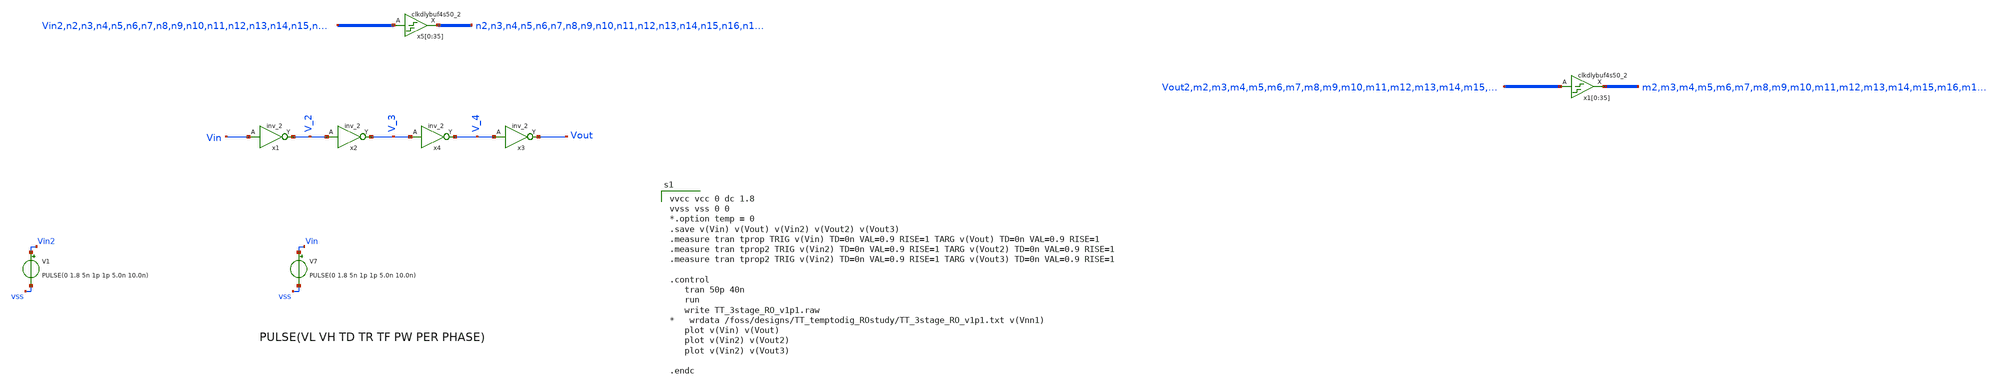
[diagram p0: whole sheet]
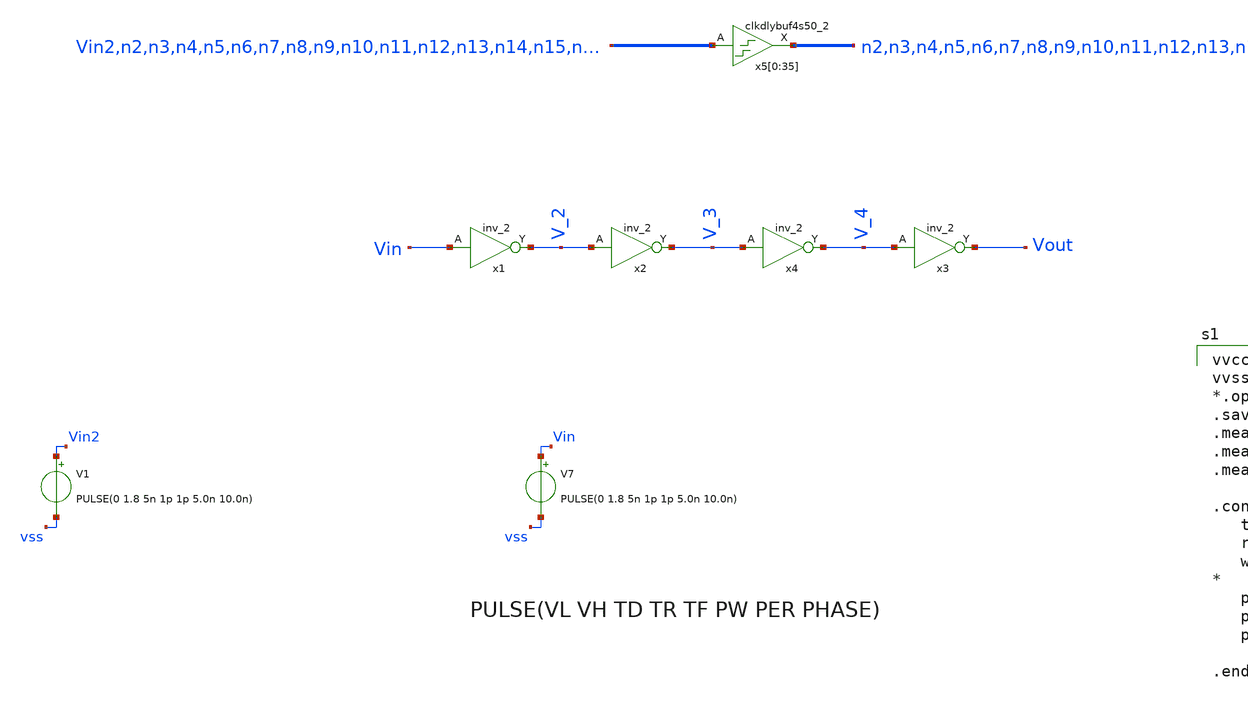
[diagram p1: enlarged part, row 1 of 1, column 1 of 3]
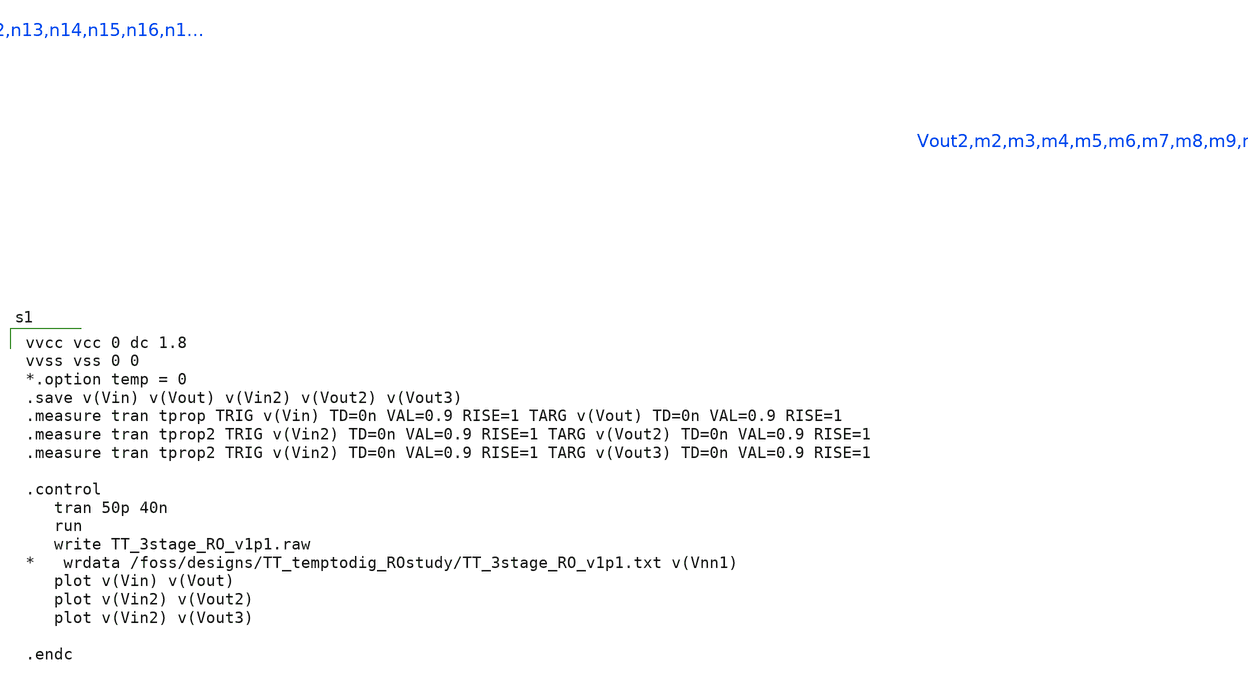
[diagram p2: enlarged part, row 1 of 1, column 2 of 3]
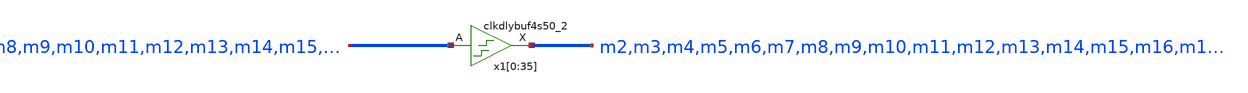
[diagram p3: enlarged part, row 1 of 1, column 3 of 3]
** sch_path: LS_boot_20230921/sch/TDC_test_buf.sch
.lib $::SKYWATER_MODELS/sky130.lib.spice tt
.include $::SKYWATER_STDCELLS/sky130_fd_sc_hd.spice

**.subckt TDC_test_buf
x1 Vin VSS VSS VCC VCC V_2 sky130_fd_sc_hd__inv_2
x2 V_2 VSS VSS VCC VCC V_3 sky130_fd_sc_hd__inv_2
x3 V_4 VSS VSS VCC VCC Vout sky130_fd_sc_hd__inv_2
V7 Vin vss PULSE(0 1.8 5n 1p 1p 5.0n 10.0n)
x4 V_3 VSS VSS VCC VCC V_4 sky130_fd_sc_hd__inv_2
V1 Vin2 vss PULSE(0 1.8 5n 1p 1p 5.0n 10.0n)
x5[0] Vin2 VSS VSS VCC VCC n2 sky130_fd_sc_hd__clkdlybuf4s50_2
x5[1] n2 VSS VSS VCC VCC n3 sky130_fd_sc_hd__clkdlybuf4s50_2
x5[2] n3 VSS VSS VCC VCC n4 sky130_fd_sc_hd__clkdlybuf4s50_2
x5[3] n4 VSS VSS VCC VCC n5 sky130_fd_sc_hd__clkdlybuf4s50_2
x5[4] n5 VSS VSS VCC VCC n6 sky130_fd_sc_hd__clkdlybuf4s50_2
x5[5] n6 VSS VSS VCC VCC n7 sky130_fd_sc_hd__clkdlybuf4s50_2
x5[6] n7 VSS VSS VCC VCC n8 sky130_fd_sc_hd__clkdlybuf4s50_2
x5[7] n8 VSS VSS VCC VCC n9 sky130_fd_sc_hd__clkdlybuf4s50_2
x5[8] n9 VSS VSS VCC VCC n10 sky130_fd_sc_hd__clkdlybuf4s50_2
x5[9] n10 VSS VSS VCC VCC n11 sky130_fd_sc_hd__clkdlybuf4s50_2
x5[10] n11 VSS VSS VCC VCC n12 sky130_fd_sc_hd__clkdlybuf4s50_2
x5[11] n12 VSS VSS VCC VCC n13 sky130_fd_sc_hd__clkdlybuf4s50_2
x5[12] n13 VSS VSS VCC VCC n14 sky130_fd_sc_hd__clkdlybuf4s50_2
x5[13] n14 VSS VSS VCC VCC n15 sky130_fd_sc_hd__clkdlybuf4s50_2
x5[14] n15 VSS VSS VCC VCC n16 sky130_fd_sc_hd__clkdlybuf4s50_2
x5[15] n16 VSS VSS VCC VCC n17 sky130_fd_sc_hd__clkdlybuf4s50_2
x5[16] n17 VSS VSS VCC VCC n18 sky130_fd_sc_hd__clkdlybuf4s50_2
x5[17] n18 VSS VSS VCC VCC n19 sky130_fd_sc_hd__clkdlybuf4s50_2
x5[18] n19 VSS VSS VCC VCC n20 sky130_fd_sc_hd__clkdlybuf4s50_2
x5[19] n20 VSS VSS VCC VCC n21 sky130_fd_sc_hd__clkdlybuf4s50_2
x5[20] n21 VSS VSS VCC VCC n22 sky130_fd_sc_hd__clkdlybuf4s50_2
x5[21] n22 VSS VSS VCC VCC n23 sky130_fd_sc_hd__clkdlybuf4s50_2
x5[22] n23 VSS VSS VCC VCC n24 sky130_fd_sc_hd__clkdlybuf4s50_2
x5[23] n24 VSS VSS VCC VCC n25 sky130_fd_sc_hd__clkdlybuf4s50_2
x5[24] n25 VSS VSS VCC VCC n26 sky130_fd_sc_hd__clkdlybuf4s50_2
x5[25] n26 VSS VSS VCC VCC n27 sky130_fd_sc_hd__clkdlybuf4s50_2
x5[26] n27 VSS VSS VCC VCC n28 sky130_fd_sc_hd__clkdlybuf4s50_2
x5[27] n28 VSS VSS VCC VCC n29 sky130_fd_sc_hd__clkdlybuf4s50_2
x5[28] n29 VSS VSS VCC VCC n30 sky130_fd_sc_hd__clkdlybuf4s50_2
x5[29] n30 VSS VSS VCC VCC n31 sky130_fd_sc_hd__clkdlybuf4s50_2
x5[30] n31 VSS VSS VCC VCC n32 sky130_fd_sc_hd__clkdlybuf4s50_2
x5[31] n32 VSS VSS VCC VCC n33 sky130_fd_sc_hd__clkdlybuf4s50_2
x5[32] n33 VSS VSS VCC VCC n34 sky130_fd_sc_hd__clkdlybuf4s50_2
x5[33] n34 VSS VSS VCC VCC n35 sky130_fd_sc_hd__clkdlybuf4s50_2
x5[34] n35 VSS VSS VCC VCC n36 sky130_fd_sc_hd__clkdlybuf4s50_2
x5[35] n36 VSS VSS VCC VCC Vout2 sky130_fd_sc_hd__clkdlybuf4s50_2
x1[0] Vout2 VSS VSS VCC VCC m2 sky130_fd_sc_hd__clkdlybuf4s50_2
x1[1] m2 VSS VSS VCC VCC m3 sky130_fd_sc_hd__clkdlybuf4s50_2
x1[2] m3 VSS VSS VCC VCC m4 sky130_fd_sc_hd__clkdlybuf4s50_2
x1[3] m4 VSS VSS VCC VCC m5 sky130_fd_sc_hd__clkdlybuf4s50_2
x1[4] m5 VSS VSS VCC VCC m6 sky130_fd_sc_hd__clkdlybuf4s50_2
x1[5] m6 VSS VSS VCC VCC m7 sky130_fd_sc_hd__clkdlybuf4s50_2
x1[6] m7 VSS VSS VCC VCC m8 sky130_fd_sc_hd__clkdlybuf4s50_2
x1[7] m8 VSS VSS VCC VCC m9 sky130_fd_sc_hd__clkdlybuf4s50_2
x1[8] m9 VSS VSS VCC VCC m10 sky130_fd_sc_hd__clkdlybuf4s50_2
x1[9] m10 VSS VSS VCC VCC m11 sky130_fd_sc_hd__clkdlybuf4s50_2
x1[10] m11 VSS VSS VCC VCC m12 sky130_fd_sc_hd__clkdlybuf4s50_2
x1[11] m12 VSS VSS VCC VCC m13 sky130_fd_sc_hd__clkdlybuf4s50_2
x1[12] m13 VSS VSS VCC VCC m14 sky130_fd_sc_hd__clkdlybuf4s50_2
x1[13] m14 VSS VSS VCC VCC m15 sky130_fd_sc_hd__clkdlybuf4s50_2
x1[14] m15 VSS VSS VCC VCC m16 sky130_fd_sc_hd__clkdlybuf4s50_2
x1[15] m16 VSS VSS VCC VCC m17 sky130_fd_sc_hd__clkdlybuf4s50_2
x1[16] m17 VSS VSS VCC VCC m18 sky130_fd_sc_hd__clkdlybuf4s50_2
x1[17] m18 VSS VSS VCC VCC m19 sky130_fd_sc_hd__clkdlybuf4s50_2
x1[18] m19 VSS VSS VCC VCC m20 sky130_fd_sc_hd__clkdlybuf4s50_2
x1[19] m20 VSS VSS VCC VCC m21 sky130_fd_sc_hd__clkdlybuf4s50_2
x1[20] m21 VSS VSS VCC VCC m22 sky130_fd_sc_hd__clkdlybuf4s50_2
x1[21] m22 VSS VSS VCC VCC m23 sky130_fd_sc_hd__clkdlybuf4s50_2
x1[22] m23 VSS VSS VCC VCC m24 sky130_fd_sc_hd__clkdlybuf4s50_2
x1[23] m24 VSS VSS VCC VCC m25 sky130_fd_sc_hd__clkdlybuf4s50_2
x1[24] m25 VSS VSS VCC VCC m26 sky130_fd_sc_hd__clkdlybuf4s50_2
x1[25] m26 VSS VSS VCC VCC m27 sky130_fd_sc_hd__clkdlybuf4s50_2
x1[26] m27 VSS VSS VCC VCC m28 sky130_fd_sc_hd__clkdlybuf4s50_2
x1[27] m28 VSS VSS VCC VCC m29 sky130_fd_sc_hd__clkdlybuf4s50_2
x1[28] m29 VSS VSS VCC VCC m30 sky130_fd_sc_hd__clkdlybuf4s50_2
x1[29] m30 VSS VSS VCC VCC m31 sky130_fd_sc_hd__clkdlybuf4s50_2
x1[30] m31 VSS VSS VCC VCC m32 sky130_fd_sc_hd__clkdlybuf4s50_2
x1[31] m32 VSS VSS VCC VCC m33 sky130_fd_sc_hd__clkdlybuf4s50_2
x1[32] m33 VSS VSS VCC VCC m34 sky130_fd_sc_hd__clkdlybuf4s50_2
x1[33] m34 VSS VSS VCC VCC m35 sky130_fd_sc_hd__clkdlybuf4s50_2
x1[34] m35 VSS VSS VCC VCC m36 sky130_fd_sc_hd__clkdlybuf4s50_2
x1[35] m36 VSS VSS VCC VCC Vout3 sky130_fd_sc_hd__clkdlybuf4s50_2
**** begin user architecture code

vvcc vcc 0 dc 1.8
vvss vss 0 0
*.option temp = 0
.save v(Vin) v(Vout) v(Vin2) v(Vout2) v(Vout3)
.measure tran tprop TRIG v(Vin) TD=0n VAL=0.9 RISE=1 TARG v(Vout) TD=0n VAL=0.9 RISE=1
.measure tran tprop2 TRIG v(Vin2) TD=0n VAL=0.9 RISE=1 TARG v(Vout2) TD=0n VAL=0.9 RISE=1
.measure tran tprop2 TRIG v(Vin2) TD=0n VAL=0.9 RISE=1 TARG v(Vout3) TD=0n VAL=0.9 RISE=1

.control
   tran 50p 40n
   run
   write TT_3stage_RO_v1p1.raw
*   wrdata /foss/designs/TT_temptodig_ROstudy/TT_3stage_RO_v1p1.txt v(Vnn1)
   plot v(Vin) v(Vout)
   plot v(Vin2) v(Vout2)
   plot v(Vin2) v(Vout3)

.endc


**** end user architecture code
**.ends
.end
